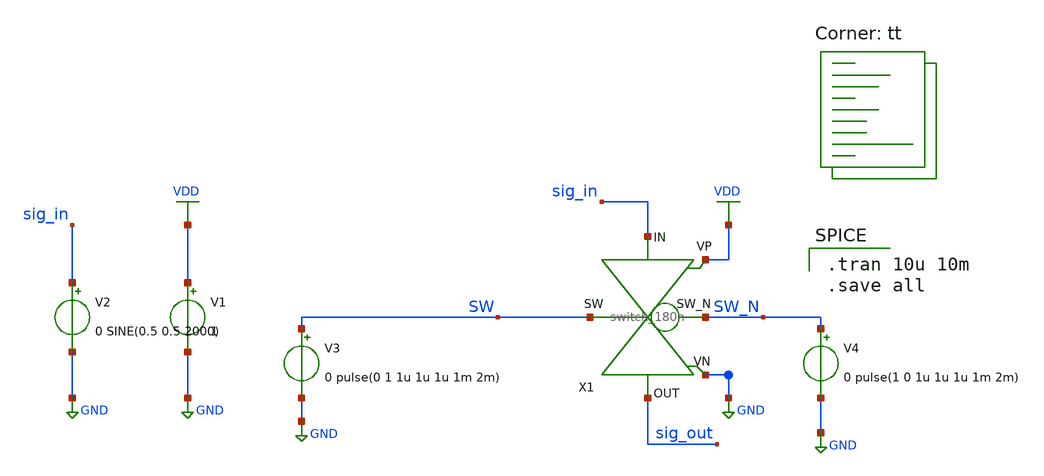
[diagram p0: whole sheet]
** sch_path: switch_180n/switch_180n_transient.sch
**.subckt switch_180n_transient
V1 VDD GND 1
V2 sig_in GND 0 SINE(0.5 0.5 2000)
V3 SW GND 0 pulse(0 1 1u 1u 1u 1m 2m)
V4 SW_N GND 0 pulse(1 0 1u 1u 1u 1m 2m)
X1 SW_N sig_in SW sig_out VDD GND switch_180n
**** begin user architecture code

.tran 10u 10m
.save all

.lib $::SKYWATER_MODELS/sky130.lib.spice tt
**** end user architecture code
**.ends
.GLOBAL GND
.GLOBAL VDD
.end
